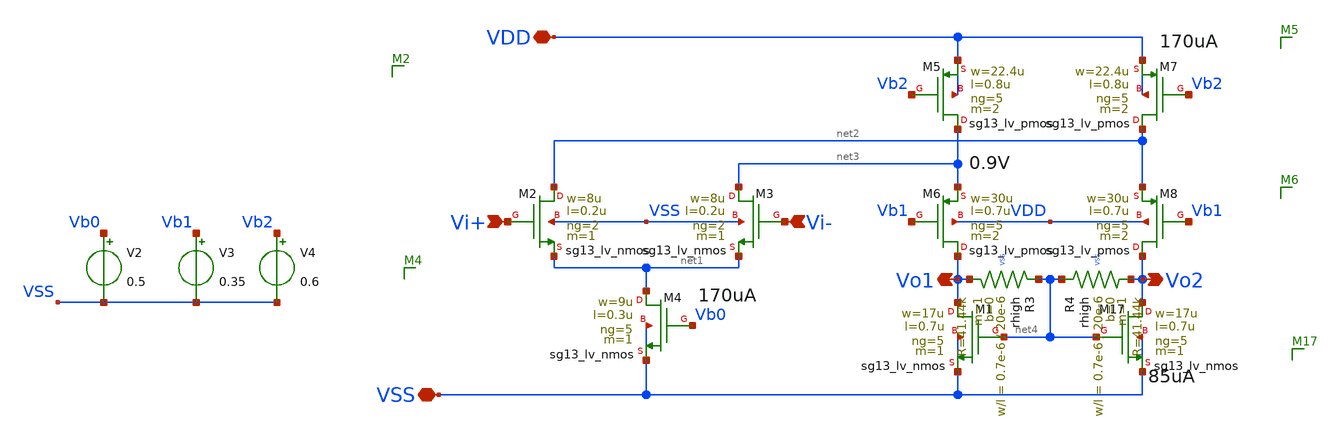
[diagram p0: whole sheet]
** sch_path: sch/blocks/gmBoostingP.sch
**.subckt gmBoostingP VDD VSS Vi+ Vi- Vo1 Vo2
*.iopin VDD
*.iopin VSS
*.ipin Vi+
*.ipin Vi-
*.opin Vo1
*.opin Vo2
V2 Vb0 VSS 0.5
V3 Vb1 VSS 0.35
V4 Vb2 VSS 0.6
XM2 net2 Vi+ net1 VSS sg13_lv_nmos w=8u l=0.2u ng=2 m=1 mm_ok=1
XM3 net3 Vi- net1 VSS sg13_lv_nmos w=8u l=0.2u ng=2 m=1 mm_ok=1
XM4 net1 Vb0 VSS VSS sg13_lv_nmos w=9u l=0.3u ng=5 m=1 mm_ok=1
XM5 net3 Vb2 VDD VDD sg13_lv_pmos w=22.4u l=0.8u ng=5 m=2 mm_ok=1
XM6 Vo1 Vb1 net3 VDD sg13_lv_pmos w=30u l=0.7u ng=5 m=2 mm_ok=1
XM7 net2 Vb2 VDD VDD sg13_lv_pmos w=22.4u l=0.8u ng=5 m=2 mm_ok=1
XM8 Vo2 Vb1 net2 VDD sg13_lv_pmos w=30u l=0.7u ng=5 m=2 mm_ok=1
XR4 net4 Vo2 VSS rhigh w=0.7e-6 l=20e-6 m=1 b=0 mm_ok=1
XM17 Vo2 net4 VSS VSS sg13_lv_nmos w=17u l=0.7u ng=5 m=1 mm_ok=1
XM1 Vo1 net4 VSS VSS sg13_lv_nmos w=17u l=0.7u ng=5 m=1 mm_ok=1
XR3 net4 Vo1 VSS rhigh w=0.7e-6 l=20e-6 m=1 b=0 mm_ok=1
**.ends
.end
